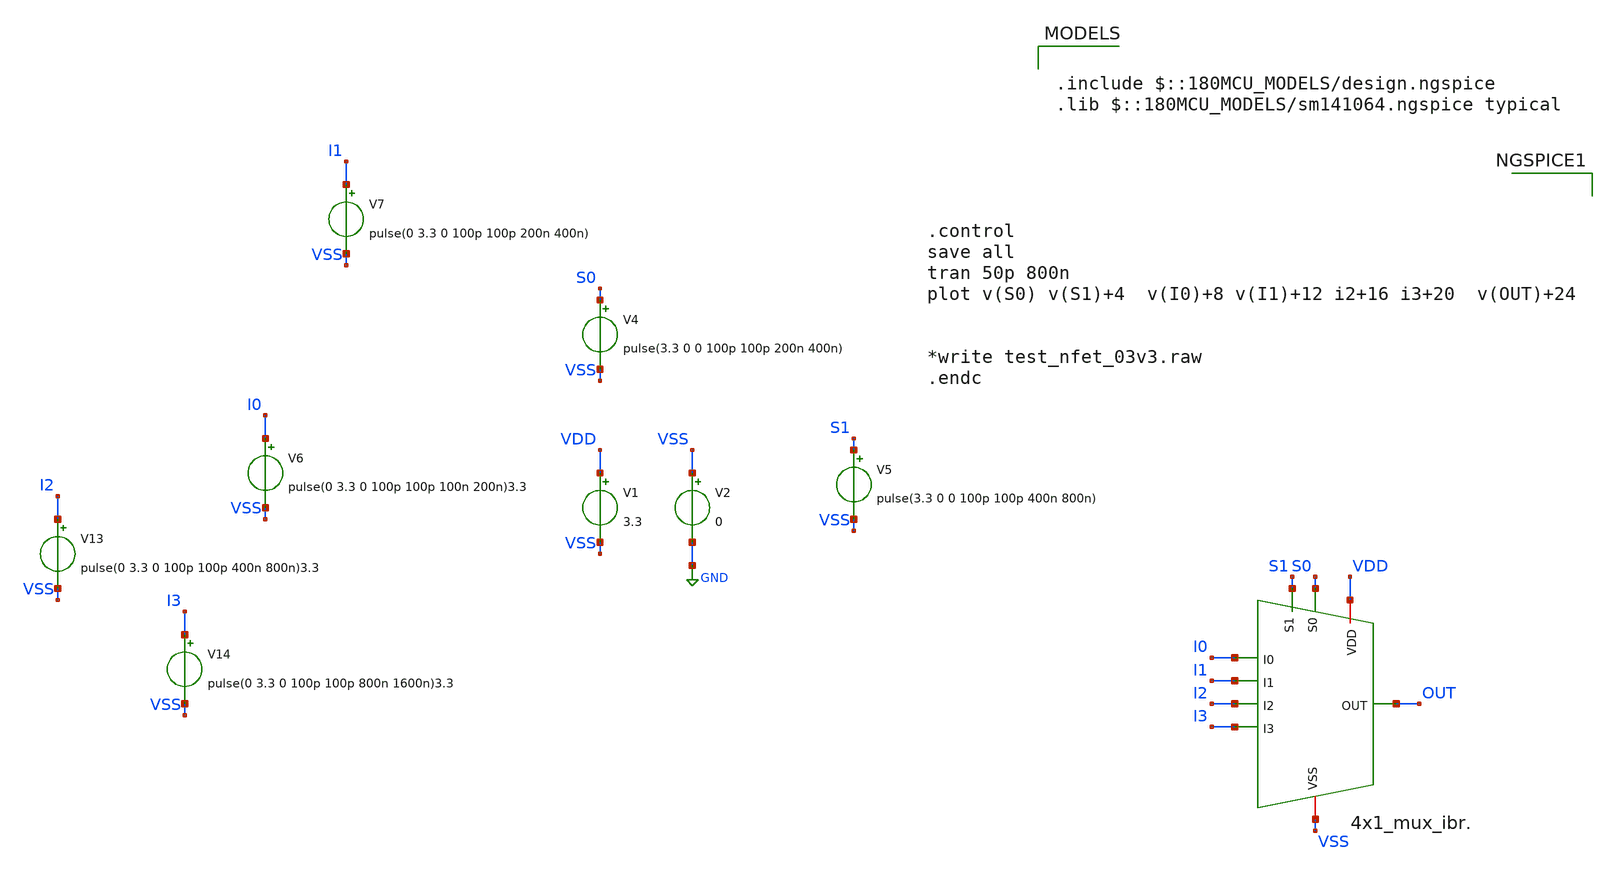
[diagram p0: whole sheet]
** sch_path: Clock_Generator_PAKISTAN_02/Schematics/4x1_mux_test_ibr..sch
**.subckt 4x1_mux_test_ibr.
V1 VDD VSS 3.3
V2 VSS GND 0
V4 S0 VSS pulse(3.3 0 0 100p 100p 200n 400n)
V6 I0 VSS pulse(0 3.3 0 100p 100p 100n 200n)3.3
V7 I1 VSS pulse(0 3.3 0 100p 100p 200n 400n)
V5 S1 VSS pulse(3.3 0 0 100p 100p 400n 800n)
V13 I2 VSS pulse(0 3.3 0 100p 100p 400n 800n)3.3
V14 I3 VSS pulse(0 3.3 0 100p 100p 800n 1600n)3.3
x1 VDD S1 VSS I2 I3 S0 I0 I1 OUT 4x1_mux_ibr.
**** begin user architecture code

.include $::180MCU_MODELS/design.ngspice
.lib $::180MCU_MODELS/sm141064.ngspice typical




.control
save all
tran 50p 800n
plot v(S0) v(S1)+4  v(I0)+8 v(I1)+12 i2+16 i3+20  v(OUT)+24


*write test_nfet_03v3.raw
.endc


**** end user architecture code
**.ends
.GLOBAL GND
.end
